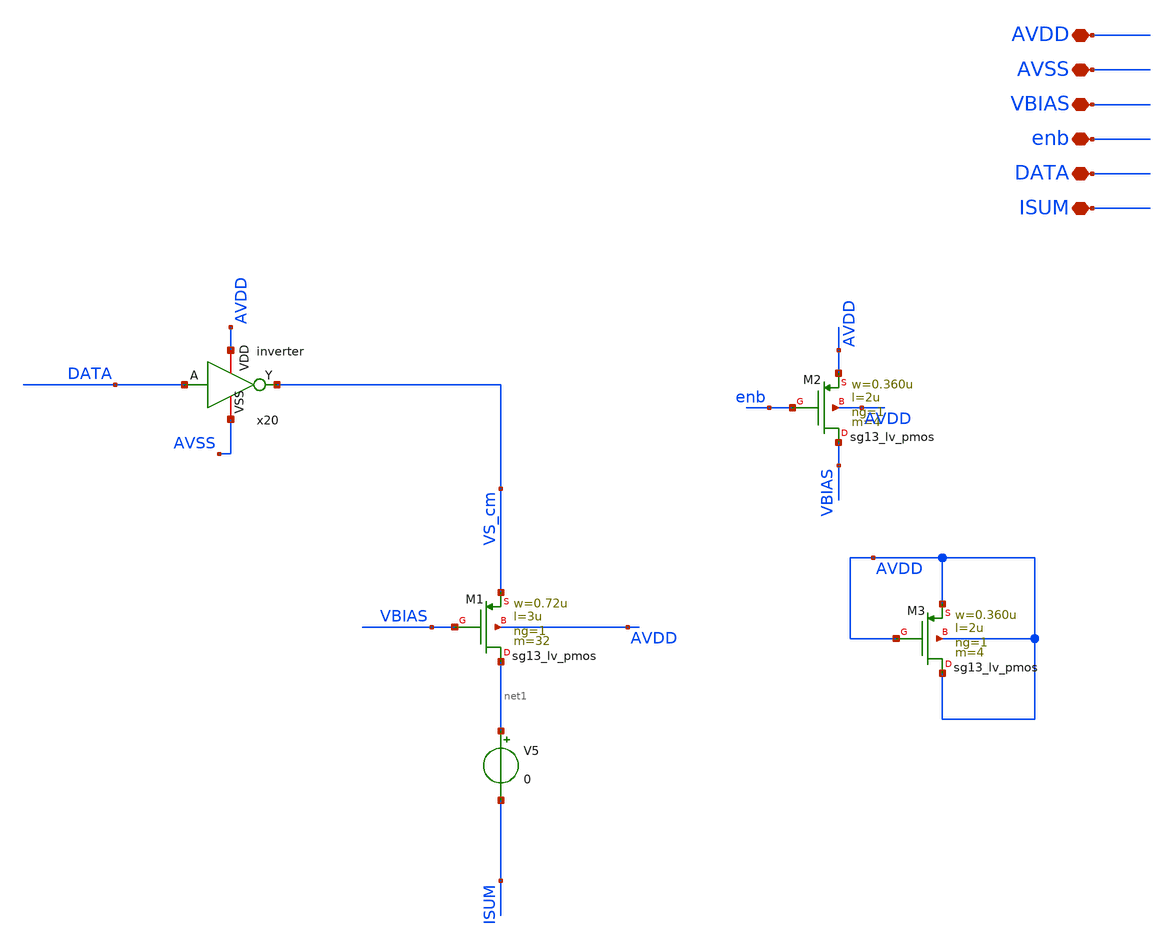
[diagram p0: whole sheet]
** sch_path: current_generator/analog/DAC/schematics/dac_thermo.sch
**.subckt dac_thermo AVDD AVSS VBIAS enb DATA ISUM
*.iopin AVDD
*.iopin AVSS
*.iopin VBIAS
*.iopin enb
*.iopin DATA
*.iopin ISUM
XM1 net1 VBIAS VS_cm AVDD sg13_lv_pmos w=0.72u l=3u ng=1 m=32 mm_ok=1
XM2 VBIAS enb AVDD AVDD sg13_lv_pmos w=0.360u l=2u ng=1 m=4 mm_ok=1
XM3 AVDD AVDD AVDD AVDD sg13_lv_pmos w=0.360u l=2u ng=1 m=4 mm_ok=1
V5 net1 ISUM 0
x20 DATA VS_cm AVDD AVSS inverter
**.ends

* expanding   symbol:  inverter.sym # of pins=4
** sym_path: current_generator/analog/DAC/schematics/inverter.sym
** sch_path: current_generator/analog/DAC/schematics/inverter.sch
.subckt inverter A Y VDD VSS
*.opin Y
*.ipin A
*.iopin VDD
*.iopin VSS
MMN0 Y A VSS VSS sg13_lv_nmos w=740.00n l=130.00n ng=1 m=1 mm_ok=1
MMP0 Y A VDD VDD sg13_lv_pmos w=1.12u l=130.00n ng=1 m=1 mm_ok=1
.ends

.end
